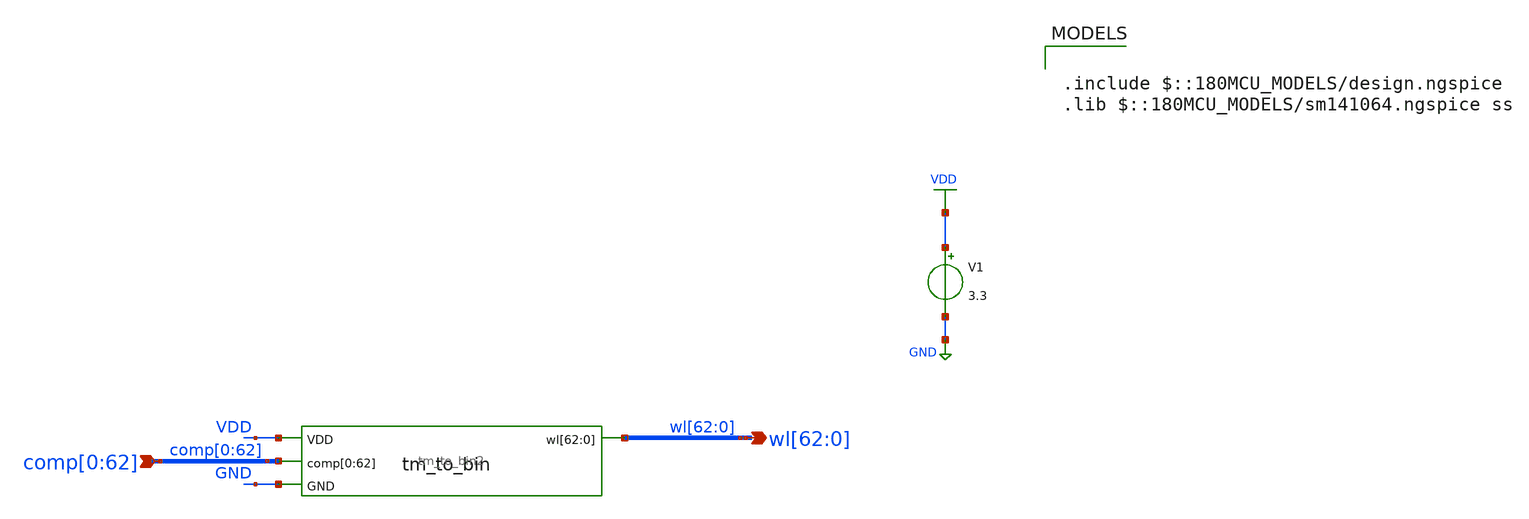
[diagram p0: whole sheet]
** sch_path: blocks/adc/encoder/tb/tm_to_oh_postlayout_tb.sch
**.subckt tm_to_oh_postlayout_tb
*+ wl[62],wl[61],wl[60],wl[59],wl[58],wl[57],wl[56],wl[55],wl[54],wl[53],wl[52],wl[51],wl[50],wl[49],wl[48],wl[47],wl[46],wl[45],wl[44],wl[43],wl[42],wl[41],wl[40],wl[39],wl[38],wl[37],wl[36],wl[35],wl[34],wl[33],wl[32],wl[31],wl[30],wl[29],wl[28],wl[27],wl[26],wl[25],wl[24],wl[23],wl[22],wl[21],wl[20],wl[19],wl[18],wl[17],wl[16],wl[15],wl[14],wl[13],wl[12],wl[11],wl[10],wl[9],wl[8],wl[7],wl[6],wl[5],wl[4],wl[3],wl[2],wl[1],wl[0]
*+ comp[0],comp[1],comp[2],comp[3],comp[4],comp[5],comp[6],comp[7],comp[8],comp[9],comp[10],comp[11],comp[12],comp[13],comp[14],comp[15],comp[16],comp[17],comp[18],comp[19],comp[20],comp[21],comp[22],comp[23],comp[24],comp[25],comp[26],comp[27],comp[28],comp[29],comp[30],comp[31],comp[32],comp[33],comp[34],comp[35],comp[36],comp[37],comp[38],comp[39],comp[40],comp[41],comp[42],comp[43],comp[44],comp[45],comp[46],comp[47],comp[48],comp[49],comp[50],comp[51],comp[52],comp[53],comp[54],comp[55],comp[56],comp[57],comp[58],comp[59],comp[60],comp[61],comp[62]
*.opin
*+ wl[62],wl[61],wl[60],wl[59],wl[58],wl[57],wl[56],wl[55],wl[54],wl[53],wl[52],wl[51],wl[50],wl[49],wl[48],wl[47],wl[46],wl[45],wl[44],wl[43],wl[42],wl[41],wl[40],wl[39],wl[38],wl[37],wl[36],wl[35],wl[34],wl[33],wl[32],wl[31],wl[30],wl[29],wl[28],wl[27],wl[26],wl[25],wl[24],wl[23],wl[22],wl[21],wl[20],wl[19],wl[18],wl[17],wl[16],wl[15],wl[14],wl[13],wl[12],wl[11],wl[10],wl[9],wl[8],wl[7],wl[6],wl[5],wl[4],wl[3],wl[2],wl[1],wl[0]
*.ipin
*+ comp[0],comp[1],comp[2],comp[3],comp[4],comp[5],comp[6],comp[7],comp[8],comp[9],comp[10],comp[11],comp[12],comp[13],comp[14],comp[15],comp[16],comp[17],comp[18],comp[19],comp[20],comp[21],comp[22],comp[23],comp[24],comp[25],comp[26],comp[27],comp[28],comp[29],comp[30],comp[31],comp[32],comp[33],comp[34],comp[35],comp[36],comp[37],comp[38],comp[39],comp[40],comp[41],comp[42],comp[43],comp[44],comp[45],comp[46],comp[47],comp[48],comp[49],comp[50],comp[51],comp[52],comp[53],comp[54],comp[55],comp[56],comp[57],comp[58],comp[59],comp[60],comp[61],comp[62]
V1 VDD GND 3.3
x1 VDD comp[0] comp[1] comp[2] comp[3] comp[4] comp[5] comp[6] comp[7] comp[8] comp[9] comp[10]
+ comp[11] comp[12] comp[13] comp[14] comp[15] comp[16] comp[17] comp[18] comp[19] comp[20] comp[21] comp[22]
+ comp[23] comp[24] comp[25] comp[26] comp[27] comp[28] comp[29] comp[30] comp[31] comp[32] comp[33] comp[34]
+ comp[35] comp[36] comp[37] comp[38] comp[39] comp[40] comp[41] comp[42] comp[43] comp[44] comp[45] comp[46]
+ comp[47] comp[48] comp[49] comp[50] comp[51] comp[52] comp[53] comp[54] comp[55] comp[56] comp[57] comp[58]
+ comp[59] comp[60] comp[61] comp[62] GND wl[62] wl[61] wl[60] wl[59] wl[58] wl[57] wl[56] wl[55] wl[54]
+ wl[53] wl[52] wl[51] wl[50] wl[49] wl[48] wl[47] wl[46] wl[45] wl[44] wl[43] wl[42] wl[41] wl[40] wl[39]
+ wl[38] wl[37] wl[36] wl[35] wl[34] wl[33] wl[32] wl[31] wl[30] wl[29] wl[28] wl[27] wl[26] wl[25] wl[24]
+ wl[23] wl[22] wl[21] wl[20] wl[19] wl[18] wl[17] wl[16] wl[15] wl[14] wl[13] wl[12] wl[11] wl[10] wl[9]
+ wl[8] wl[7] wl[6] wl[5] wl[4] wl[3] wl[2] wl[1] wl[0] tm_to_bin2
**** begin user architecture code

.include $::180MCU_MODELS/design.ngspice
.lib $::180MCU_MODELS/sm141064.ngspice ss



.include /foss/designs/encoder/spice/tm_to_bin2.spice
V_C0 comp[0] 0 PWL(0 0 0.50n 0 0.51n 3.3)
V_C1 comp[1] 0 PWL(0 0 1.00n 0 1.01n 3.3)
V_C2 comp[2] 0 PWL(0 0 1.50n 0 1.51n 3.3)
V_C3 comp[3] 0 PWL(0 0 2.00n 0 2.01n 3.3)
V_C4 comp[4] 0 PWL(0 0 2.50n 0 2.51n 3.3)
V_C5 comp[5] 0 PWL(0 0 3.00n 0 3.01n 3.3)
V_C6 comp[6] 0 PWL(0 0 3.50n 0 3.51n 3.3)
V_C7 comp[7] 0 PWL(0 0 4.00n 0 4.01n 3.3)
V_C8 comp[8] 0 PWL(0 0 4.50n 0 4.51n 3.3)
V_C9 comp[9] 0 PWL(0 0 5.00n 0 5.01n 3.3)
V_C10 comp[10] 0 PWL(0 0 5.50n 0 5.51n 3.3)
V_C11 comp[11] 0 PWL(0 0 6.00n 0 6.01n 3.3)
V_C12 comp[12] 0 PWL(0 0 6.50n 0 6.51n 3.3)
V_C13 comp[13] 0 PWL(0 0 7.00n 0 7.01n 3.3)
V_C14 comp[14] 0 PWL(0 0 7.50n 0 7.51n 3.3)
V_C15 comp[15] 0 PWL(0 0 8.00n 0 8.01n 3.3)
V_C16 comp[16] 0 PWL(0 0 8.50n 0 8.51n 3.3)
V_C17 comp[17] 0 PWL(0 0 9.00n 0 9.01n 3.3)
V_C18 comp[18] 0 PWL(0 0 9.50n 0 9.51n 3.3)
V_C19 comp[19] 0 PWL(0 0 10.00n 0 10.01n 3.3)
V_C20 comp[20] 0 PWL(0 0 10.50n 0 10.51n 3.3)
V_C21 comp[21] 0 PWL(0 0 11.00n 0 11.01n 3.3)
V_C22 comp[22] 0 PWL(0 0 11.50n 0 11.51n 3.3)
V_C23 comp[23] 0 PWL(0 0 12.00n 0 12.01n 3.3)
V_C24 comp[24] 0 PWL(0 0 12.50n 0 12.51n 3.3)
V_C25 comp[25] 0 PWL(0 0 13.00n 0 13.01n 3.3)
V_C26 comp[26] 0 PWL(0 0 13.50n 0 13.51n 3.3)
V_C27 comp[27] 0 PWL(0 0 14.00n 0 14.01n 3.3)
V_C28 comp[28] 0 PWL(0 0 14.50n 0 14.51n 3.3)
V_C29 comp[29] 0 PWL(0 0 15.00n 0 15.01n 3.3)
V_C30 comp[30] 0 PWL(0 0 15.50n 0 15.51n 3.3)
V_C31 comp[31] 0 PWL(0 0 16.00n 0 16.01n 3.3)
V_C32 comp[32] 0 PWL(0 0 16.50n 0 16.51n 3.3)
V_C33 comp[33] 0 PWL(0 0 17.00n 0 17.01n 3.3)
V_C34 comp[34] 0 PWL(0 0 17.50n 0 17.51n 3.3)
V_C35 comp[35] 0 PWL(0 0 18.00n 0 18.01n 3.3)
V_C36 comp[36] 0 PWL(0 0 18.50n 0 18.51n 3.3)
V_C37 comp[37] 0 PWL(0 0 19.00n 0 19.01n 3.3)
V_C38 comp[38] 0 PWL(0 0 19.50n 0 19.51n 3.3)
V_C39 comp[39] 0 PWL(0 0 20.00n 0 20.01n 3.3)
V_C40 comp[40] 0 PWL(0 0 20.50n 0 20.51n 3.3)
V_C41 comp[41] 0 PWL(0 0 21.00n 0 21.01n 3.3)
V_C42 comp[42] 0 PWL(0 0 21.50n 0 21.51n 3.3)
V_C43 comp[43] 0 PWL(0 0 22.00n 0 22.01n 3.3)
V_C44 comp[44] 0 PWL(0 0 22.50n 0 22.51n 3.3)
V_C45 comp[45] 0 PWL(0 0 23.00n 0 23.01n 3.3)
V_C46 comp[46] 0 PWL(0 0 23.50n 0 23.51n 3.3)
V_C47 comp[47] 0 PWL(0 0 24.00n 0 24.01n 3.3)
V_C48 comp[48] 0 PWL(0 0 24.50n 0 24.51n 3.3)
V_C49 comp[49] 0 PWL(0 0 25.00n 0 25.01n 3.3)
V_C50 comp[50] 0 PWL(0 0 25.50n 0 25.51n 3.3)
V_C51 comp[51] 0 PWL(0 0 26.00n 0 26.01n 3.3)
V_C52 comp[52] 0 PWL(0 0 26.50n 0 26.51n 3.3)
V_C53 comp[53] 0 PWL(0 0 27.00n 0 27.01n 3.3)
V_C54 comp[54] 0 PWL(0 0 27.50n 0 27.51n 3.3)
V_C55 comp[55] 0 PWL(0 0 28.00n 0 28.01n 3.3)
V_C56 comp[56] 0 PWL(0 0 28.50n 0 28.51n 3.3)
V_C57 comp[57] 0 PWL(0 0 29.00n 0 29.01n 3.3)
V_C58 comp[58] 0 PWL(0 0 29.50n 0 29.51n 3.3)
V_C59 comp[59] 0 PWL(0 0 30.00n 0 30.01n 3.3)
V_C60 comp[60] 0 PWL(0 0 30.50n 0 30.51n 3.3)
V_C61 comp[61] 0 PWL(0 0 31.00n 0 31.01n 3.3)
V_C62 comp[62] 0 PWL(0 0 31.50n 0 31.51n 3.3)

.tran 10p 6n uic

.control
  run
  write full_decoder_test.raw
.endc


**** end user architecture code
**.ends

* expanding   symbol:  encoder/sym/tm_to_bin2.sym # of pins=4
** sym_path: blocks/adc/encoder/tm_to_bin2.sym
** sch_path: blocks/adc/encoder/tm_to_bin2.sch
.subckt tm_to_bin2 VDD comp[0] comp[1] comp[2] comp[3] comp[4] comp[5] comp[6] comp[7] comp[8]
+ comp[9] comp[10] comp[11] comp[12] comp[13] comp[14] comp[15] comp[16] comp[17] comp[18] comp[19] comp[20]
+ comp[21] comp[22] comp[23] comp[24] comp[25] comp[26] comp[27] comp[28] comp[29] comp[30] comp[31] comp[32]
+ comp[33] comp[34] comp[35] comp[36] comp[37] comp[38] comp[39] comp[40] comp[41] comp[42] comp[43] comp[44]
+ comp[45] comp[46] comp[47] comp[48] comp[49] comp[50] comp[51] comp[52] comp[53] comp[54] comp[55] comp[56]
+ comp[57] comp[58] comp[59] comp[60] comp[61] comp[62] GND wl[62] wl[61] wl[60] wl[59] wl[58] wl[57] wl[56]
+ wl[55] wl[54] wl[53] wl[52] wl[51] wl[50] wl[49] wl[48] wl[47] wl[46] wl[45] wl[44] wl[43] wl[42] wl[41]
+ wl[40] wl[39] wl[38] wl[37] wl[36] wl[35] wl[34] wl[33] wl[32] wl[31] wl[30] wl[29] wl[28] wl[27] wl[26]
+ wl[25] wl[24] wl[23] wl[22] wl[21] wl[20] wl[19] wl[18] wl[17] wl[16] wl[15] wl[14] wl[13] wl[12] wl[11]
+ wl[10] wl[9] wl[8] wl[7] wl[6] wl[5] wl[4] wl[3] wl[2] wl[1] wl[0]
*.opin
*+ wl[62],wl[61],wl[60],wl[59],wl[58],wl[57],wl[56],wl[55],wl[54],wl[53],wl[52],wl[51],wl[50],wl[49],wl[48],wl[47],wl[46],wl[45],wl[44],wl[43],wl[42],wl[41],wl[40],wl[39],wl[38],wl[37],wl[36],wl[35],wl[34],wl[33],wl[32],wl[31],wl[30],wl[29],wl[28],wl[27],wl[26],wl[25],wl[24],wl[23],wl[22],wl[21],wl[20],wl[19],wl[18],wl[17],wl[16],wl[15],wl[14],wl[13],wl[12],wl[11],wl[10],wl[9],wl[8],wl[7],wl[6],wl[5],wl[4],wl[3],wl[2],wl[1],wl[0]
*.ipin
*+ comp[0],comp[1],comp[2],comp[3],comp[4],comp[5],comp[6],comp[7],comp[8],comp[9],comp[10],comp[11],comp[12],comp[13],comp[14],comp[15],comp[16],comp[17],comp[18],comp[19],comp[20],comp[21],comp[22],comp[23],comp[24],comp[25],comp[26],comp[27],comp[28],comp[29],comp[30],comp[31],comp[32],comp[33],comp[34],comp[35],comp[36],comp[37],comp[38],comp[39],comp[40],comp[41],comp[42],comp[43],comp[44],comp[45],comp[46],comp[47],comp[48],comp[49],comp[50],comp[51],comp[52],comp[53],comp[54],comp[55],comp[56],comp[57],comp[58],comp[59],comp[60],comp[61],comp[62]
*.ipin VDD
*.ipin GND
x1[61] comp[1] comp[0] VDD wl[1] comp[2] GND NAND3
x1[60] comp[2] comp[1] VDD wl[2] comp[3] GND NAND3
x1[59] comp[3] comp[2] VDD wl[3] comp[4] GND NAND3
x1[58] comp[4] comp[3] VDD wl[4] comp[5] GND NAND3
x1[57] comp[5] comp[4] VDD wl[5] comp[6] GND NAND3
x1[56] comp[6] comp[5] VDD wl[6] comp[7] GND NAND3
x1[55] comp[7] comp[6] VDD wl[7] comp[8] GND NAND3
x1[54] comp[8] comp[7] VDD wl[8] comp[9] GND NAND3
x1[53] comp[9] comp[8] VDD wl[9] comp[10] GND NAND3
x1[52] comp[10] comp[9] VDD wl[10] comp[11] GND NAND3
x1[51] comp[11] comp[10] VDD wl[11] comp[12] GND NAND3
x1[50] comp[12] comp[11] VDD wl[12] comp[13] GND NAND3
x1[49] comp[13] comp[12] VDD wl[13] comp[14] GND NAND3
x1[48] comp[14] comp[13] VDD wl[14] comp[15] GND NAND3
x1[47] comp[15] comp[14] VDD wl[15] comp[16] GND NAND3
x1[46] comp[16] comp[15] VDD wl[16] comp[17] GND NAND3
x1[45] comp[17] comp[16] VDD wl[17] comp[18] GND NAND3
x1[44] comp[18] comp[17] VDD wl[18] comp[19] GND NAND3
x1[43] comp[19] comp[18] VDD wl[19] comp[20] GND NAND3
x1[42] comp[20] comp[19] VDD wl[20] comp[21] GND NAND3
x1[41] comp[21] comp[20] VDD wl[21] comp[22] GND NAND3
x1[40] comp[22] comp[21] VDD wl[22] comp[23] GND NAND3
x1[39] comp[23] comp[22] VDD wl[23] comp[24] GND NAND3
x1[38] comp[24] comp[23] VDD wl[24] comp[25] GND NAND3
x1[37] comp[25] comp[24] VDD wl[25] comp[26] GND NAND3
x1[36] comp[26] comp[25] VDD wl[26] comp[27] GND NAND3
x1[35] comp[27] comp[26] VDD wl[27] comp[28] GND NAND3
x1[34] comp[28] comp[27] VDD wl[28] comp[29] GND NAND3
x1[33] comp[29] comp[28] VDD wl[29] comp[30] GND NAND3
x1[32] comp[30] comp[29] VDD wl[30] comp[31] GND NAND3
x1[31] comp[31] comp[30] VDD wl[31] comp[32] GND NAND3
x1[30] comp[32] comp[31] VDD wl[32] comp[33] GND NAND3
x1[29] comp[33] comp[32] VDD wl[33] comp[34] GND NAND3
x1[28] comp[34] comp[33] VDD wl[34] comp[35] GND NAND3
x1[27] comp[35] comp[34] VDD wl[35] comp[36] GND NAND3
x1[26] comp[36] comp[35] VDD wl[36] comp[37] GND NAND3
x1[25] comp[37] comp[36] VDD wl[37] comp[38] GND NAND3
x1[24] comp[38] comp[37] VDD wl[38] comp[39] GND NAND3
x1[23] comp[39] comp[38] VDD wl[39] comp[40] GND NAND3
x1[22] comp[40] comp[39] VDD wl[40] comp[41] GND NAND3
x1[21] comp[41] comp[40] VDD wl[41] comp[42] GND NAND3
x1[20] comp[42] comp[41] VDD wl[42] comp[43] GND NAND3
x1[19] comp[43] comp[42] VDD wl[43] comp[44] GND NAND3
x1[18] comp[44] comp[43] VDD wl[44] comp[45] GND NAND3
x1[17] comp[45] comp[44] VDD wl[45] comp[46] GND NAND3
x1[16] comp[46] comp[45] VDD wl[46] comp[47] GND NAND3
x1[15] comp[47] comp[46] VDD wl[47] comp[48] GND NAND3
x1[14] comp[48] comp[47] VDD wl[48] comp[49] GND NAND3
x1[13] comp[49] comp[48] VDD wl[49] comp[50] GND NAND3
x1[12] comp[50] comp[49] VDD wl[50] comp[51] GND NAND3
x1[11] comp[51] comp[50] VDD wl[51] comp[52] GND NAND3
x1[10] comp[52] comp[51] VDD wl[52] comp[53] GND NAND3
x1[9] comp[53] comp[52] VDD wl[53] comp[54] GND NAND3
x1[8] comp[54] comp[53] VDD wl[54] comp[55] GND NAND3
x1[7] comp[55] comp[54] VDD wl[55] comp[56] GND NAND3
x1[6] comp[56] comp[55] VDD wl[56] comp[57] GND NAND3
x1[5] comp[57] comp[56] VDD wl[57] comp[58] GND NAND3
x1[4] comp[58] comp[57] VDD wl[58] comp[59] GND NAND3
x1[3] comp[59] comp[58] VDD wl[59] comp[60] GND NAND3
x1[2] comp[60] comp[59] VDD wl[60] comp[61] GND NAND3
x1[1] comp[61] comp[60] VDD wl[61] comp[62] GND NAND3
x_bot comp[0] VDD VDD wl[0] comp[1] GND NAND3
x_top comp[62] comp[61] VDD wl[62] GND GND NAND3
.ends


* expanding   symbol:  NAND3.sym # of pins=6
** sym_path: blocks/adc/encoder/sym/NAND3.sym
** sch_path: blocks/adc/encoder/sym/NAND3.sch
.subckt NAND3 b a VDD out C GND
*.ipin a
*.opin out
*.ipin C
*.ipin b
*.ipin VDD
*.ipin GND
XM5 out net1 VDD VDD pfet_03v3 L=0.28u W=3.3u nf=5 ad='int((nf+1)/2) * W/nf * 0.18u' as='int((nf+2)/2) * W/nf * 0.18u'
+ pd='2*int((nf+1)/2) * (W/nf + 0.18u)' ps='2*int((nf+2)/2) * (W/nf + 0.18u)' nrd='0.18u / W' nrs='0.18u / W'
+ sa=0 sb=0 sd=0 m=1
XM6 out net1 GND GND nfet_03v3 L=0.28u W=2.54u nf=4 ad='int((nf+1)/2) * W/nf * 0.18u' as='int((nf+2)/2) * W/nf * 0.18u'
+ pd='2*int((nf+1)/2) * (W/nf + 0.18u)' ps='2*int((nf+2)/2) * (W/nf + 0.18u)' nrd='0.18u / W' nrs='0.18u / W'
+ sa=0 sb=0 sd=0 m=1
XM7 cbar C VDD VDD pfet_03v3 L=0.28u W=3.3u nf=5 ad='int((nf+1)/2) * W/nf * 0.18u' as='int((nf+2)/2) * W/nf * 0.18u'
+ pd='2*int((nf+1)/2) * (W/nf + 0.18u)' ps='2*int((nf+2)/2) * (W/nf + 0.18u)' nrd='0.18u / W' nrs='0.18u / W'
+ sa=0 sb=0 sd=0 m=1
XM8 cbar C GND GND nfet_03v3 L=0.28u W=2.54u nf=4 ad='int((nf+1)/2) * W/nf * 0.18u' as='int((nf+2)/2) * W/nf * 0.18u'
+ pd='2*int((nf+1)/2) * (W/nf + 0.18u)' ps='2*int((nf+2)/2) * (W/nf + 0.18u)' nrd='0.18u / W' nrs='0.18u / W'
+ sa=0 sb=0 sd=0 m=1
XM13 net1 a VDD VDD pfet_03v3 L=0.28u W=3.3u nf=5 ad='int((nf+1)/2) * W/nf * 0.18u' as='int((nf+2)/2) * W/nf * 0.18u'
+ pd='2*int((nf+1)/2) * (W/nf + 0.18u)' ps='2*int((nf+2)/2) * (W/nf + 0.18u)' nrd='0.18u / W' nrs='0.18u / W'
+ sa=0 sb=0 sd=0 m=1
XM14 net1 b VDD VDD pfet_03v3 L=0.28u W=3.3u nf=5 ad='int((nf+1)/2) * W/nf * 0.18u' as='int((nf+2)/2) * W/nf * 0.18u'
+ pd='2*int((nf+1)/2) * (W/nf + 0.18u)' ps='2*int((nf+2)/2) * (W/nf + 0.18u)' nrd='0.18u / W' nrs='0.18u / W'
+ sa=0 sb=0 sd=0 m=1
XM15 net1 cbar VDD VDD pfet_03v3 L=0.28u W=3.3u nf=5 ad='int((nf+1)/2) * W/nf * 0.18u' as='int((nf+2)/2) * W/nf * 0.18u'
+ pd='2*int((nf+1)/2) * (W/nf + 0.18u)' ps='2*int((nf+2)/2) * (W/nf + 0.18u)' nrd='0.18u / W' nrs='0.18u / W'
+ sa=0 sb=0 sd=0 m=1
XM16 net1 a net2 GND nfet_03v3 L=0.28u W=2.54u nf=4 ad='int((nf+1)/2) * W/nf * 0.18u' as='int((nf+2)/2) * W/nf * 0.18u'
+ pd='2*int((nf+1)/2) * (W/nf + 0.18u)' ps='2*int((nf+2)/2) * (W/nf + 0.18u)' nrd='0.18u / W' nrs='0.18u / W'
+ sa=0 sb=0 sd=0 m=1
XM17 net2 b net3 GND nfet_03v3 L=0.28u W=2.54u nf=4 ad='int((nf+1)/2) * W/nf * 0.18u' as='int((nf+2)/2) * W/nf * 0.18u'
+ pd='2*int((nf+1)/2) * (W/nf + 0.18u)' ps='2*int((nf+2)/2) * (W/nf + 0.18u)' nrd='0.18u / W' nrs='0.18u / W'
+ sa=0 sb=0 sd=0 m=1
XM18 net3 cbar GND GND nfet_03v3 L=0.28u W=2.54u nf=4 ad='int((nf+1)/2) * W/nf * 0.18u' as='int((nf+2)/2) * W/nf * 0.18u'
+ pd='2*int((nf+1)/2) * (W/nf + 0.18u)' ps='2*int((nf+2)/2) * (W/nf + 0.18u)' nrd='0.18u / W' nrs='0.18u / W'
+ sa=0 sb=0 sd=0 m=1
.ends

.GLOBAL VDD
.GLOBAL GND
.end
